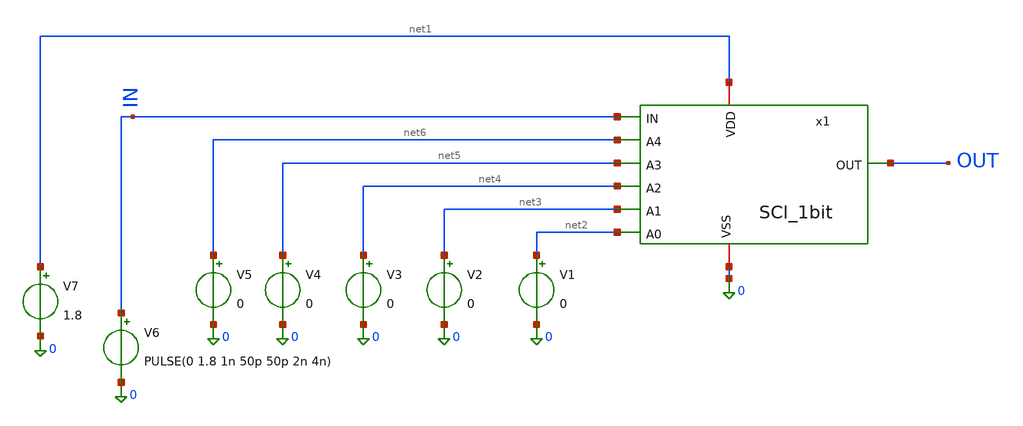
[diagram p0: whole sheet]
** sch_path: xschem/schematic/SCI_DCDL/TG_SCI/TB_SCI_MOS.sch
**.subckt TB_SCI_MOS
x1 net1 IN OUT 0 net6 net5 net4 net3 net2 SCI_1bit
V1 net2 0 0
V2 net3 0 0
V3 net4 0 0
V4 net5 0 0
V5 net6 0 0
V6 IN 0 PULSE(0 1.8 1n 50p 50p 2n 4n)
V7 net1 0 1.8
**** begin user architecture code

** opencircuitdesign pdks install
.lib $::SKYWATER_MODELS/sky130.lib.spice tt



.option rshunt=1e12
.tran 2p 25n

.control
save v(IN) v(OUT)

* Output file
echo code t_rise_ps t_fall_ps t_pd_ps > /home/xiaohi/Projects/sky130_dcdl/results/csv/sci5_delay.dat

* Sweep 5-bit: 00000 -> 11111
foreach b4 0 1
 foreach b3 0 1
  foreach b2 0 1
   foreach b1 0 1
    foreach b0 0 1

     * Convert bits to voltage
     let v0 = 1.8 * $b0
     let v1 = 1.8 * $b1
     let v2 = 1.8 * $b2
     let v3 = 1.8 * $b3
     let v4 = 1.8 * $b4

     * Set control voltage
     alter V1 $&v0
     alter V2 $&v1
     alter V3 $&v2
     alter V4 $&v3
     alter V5 $&v4

     * Run transient simulation
     run

     * Measure propagation delay
     meas tran t_rise TRIG v(IN) VAL=0.9 RISE=2 TARG v(OUT) VAL=0.9 RISE=2
     meas tran t_fall TRIG v(IN) VAL=0.9 FALL=2 TARG v(OUT) VAL=0.9 FALL=2

     * Calculate code and delay in ps
     let code = 16 * $b4 + 8 * $b3 + 4 * $b2 + 2 * $b1 + $b0
     let rise_ps = t_rise * 1e12
     let fall_ps = t_fall * 1e12
     let pd_ps = (rise_ps + fall_ps)/2

     * Append result to file
     echo $&code $&rise_ps $&fall_ps $&pd_ps >>
+ /home/xiaohi/Projects/sky130_dcdl/results/csv/sci5_delay.dat

    end
   end
  end
 end
end

echo Sweep completed: 32 codes
.endc


**** end user architecture code
**.ends

* expanding   symbol:  /home/xiaohi/Projects/sky130_dcdl/xschem/schematic/SCI_DCDL/SCI_1bit.sym # of
*+ pins=9
** sym_path: xschem/schematic/SCI_DCDL/mos_capacitive_baseline/SCI_1bit.sym
** sch_path: xschem/schematic/SCI_DCDL/mos_capacitive_baseline/SCI_1bit.sch
.subckt SCI_1bit VDD IN OUT VSS A4 A3 A2 A1 A0
*.ipin IN
*.opin OUT
*.iopin VDD
*.iopin VSS
*.ipin A4
*.ipin A3
*.ipin A2
*.ipin A1
*.ipin A0
XM1 net1 IN VSS VSS sky130_fd_pr__nfet_01v8 L=0.15 W=2 nf=1 ad='int((1 + 1)/2) * 2 / 1 * 0.29' as='int((1 + 2)/2) * 2 / 1 * 0.29'
+ pd='2*int((1 + 1)/2) * (2 / 1 + 0.29)' ps='2*int((1 + 2)/2) * (2 / 1 + 0.29)' nrd='0.29 / 2 ' nrs='0.29 / 2 '
+ sa=0 sb=0 sd=0 mult=1 m=1
XM3 OUT net1 VSS VSS sky130_fd_pr__nfet_01v8 L=0.15 W=1 nf=1 ad='int((1 + 1)/2) * 1 / 1 * 0.29' as='int((1 + 2)/2) * 1 / 1 * 0.29'
+ pd='2*int((1 + 1)/2) * (1 / 1 + 0.29)' ps='2*int((1 + 2)/2) * (1 / 1 + 0.29)' nrd='0.29 / 1 ' nrs='0.29 / 1 '
+ sa=0 sb=0 sd=0 mult=1 m=1
XM5 net1 IN VDD VDD sky130_fd_pr__pfet_01v8 L=0.15 W=5 nf=1 ad='int((1 + 1)/2) * 5 / 1 * 0.29' as='int((1 + 2)/2) * 5 / 1 * 0.29'
+ pd='2*int((1 + 1)/2) * (5 / 1 + 0.29)' ps='2*int((1 + 2)/2) * (5 / 1 + 0.29)' nrd='0.29 / 5 ' nrs='0.29 / 5 '
+ sa=0 sb=0 sd=0 mult=1 m=1
XM2 OUT net1 VDD VDD sky130_fd_pr__pfet_01v8 L=0.15 W=2.5 nf=1 ad='int((1 + 1)/2) * 2.5 / 1 * 0.29' as='int((1 + 2)/2) * 2.5 / 1 * 0.29'
+ pd='2*int((1 + 1)/2) * (2.5 / 1 + 0.29)' ps='2*int((1 + 2)/2) * (2.5 / 1 + 0.29)' nrd='0.29 / 2.5 ' nrs='0.29 / 2.5 '
+ sa=0 sb=0 sd=0 mult=1 m=1
XM4 net1 A4 net2 VSS sky130_fd_pr__nfet_01v8 L=0.15 W=0.42 nf=1 ad='int((1 + 1)/2) * 0.42 / 1 * 0.29'
+ as='int((1 + 2)/2) * 0.42 / 1 * 0.29' pd='2*int((1 + 1)/2) * (0.42 / 1 + 0.29)' ps='2*int((1 + 2)/2) * (0.42 / 1 + 0.29)'
+ nrd='0.29 / 0.42 ' nrs='0.29 / 0.42 ' sa=0 sb=0 sd=0 mult=1 m=1
XM6 net1 A3 net3 VSS sky130_fd_pr__nfet_01v8 L=0.15 W=0.42 nf=1 ad='int((1 + 1)/2) * 0.42 / 1 * 0.29'
+ as='int((1 + 2)/2) * 0.42 / 1 * 0.29' pd='2*int((1 + 1)/2) * (0.42 / 1 + 0.29)' ps='2*int((1 + 2)/2) * (0.42 / 1 + 0.29)'
+ nrd='0.29 / 0.42 ' nrs='0.29 / 0.42 ' sa=0 sb=0 sd=0 mult=1 m=1
XM7 net1 A2 net4 VSS sky130_fd_pr__nfet_01v8 L=0.15 W=0.42 nf=1 ad='int((1 + 1)/2) * 0.42 / 1 * 0.29'
+ as='int((1 + 2)/2) * 0.42 / 1 * 0.29' pd='2*int((1 + 1)/2) * (0.42 / 1 + 0.29)' ps='2*int((1 + 2)/2) * (0.42 / 1 + 0.29)'
+ nrd='0.29 / 0.42 ' nrs='0.29 / 0.42 ' sa=0 sb=0 sd=0 mult=1 m=1
XM8 net1 A1 net5 VSS sky130_fd_pr__nfet_01v8 L=0.15 W=0.42 nf=1 ad='int((1 + 1)/2) * 0.42 / 1 * 0.29'
+ as='int((1 + 2)/2) * 0.42 / 1 * 0.29' pd='2*int((1 + 1)/2) * (0.42 / 1 + 0.29)' ps='2*int((1 + 2)/2) * (0.42 / 1 + 0.29)'
+ nrd='0.29 / 0.42 ' nrs='0.29 / 0.42 ' sa=0 sb=0 sd=0 mult=1 m=1
XM9 net1 A0 net6 VSS sky130_fd_pr__nfet_01v8 L=0.15 W=0.42 nf=1 ad='int((1 + 1)/2) * 0.42 / 1 * 0.29'
+ as='int((1 + 2)/2) * 0.42 / 1 * 0.29' pd='2*int((1 + 1)/2) * (0.42 / 1 + 0.29)' ps='2*int((1 + 2)/2) * (0.42 / 1 + 0.29)'
+ nrd='0.29 / 0.42 ' nrs='0.29 / 0.42 ' sa=0 sb=0 sd=0 mult=1 m=1
XM10 VSS net2 VSS VSS sky130_fd_pr__nfet_01v8 L=0.15 W=8 nf=1 ad='int((1 + 1)/2) * 8 / 1 * 0.29' as='int((1 + 2)/2) * 8 / 1 * 0.29'
+ pd='2*int((1 + 1)/2) * (8 / 1 + 0.29)' ps='2*int((1 + 2)/2) * (8 / 1 + 0.29)' nrd='0.29 / 8 ' nrs='0.29 / 8 '
+ sa=0 sb=0 sd=0 mult=1 m=1
XM11 net7 net3 net7 net7 sky130_fd_pr__nfet_01v8 L=0.15 W=4 nf=1 ad='int((1 + 1)/2) * 4 / 1 * 0.29' as='int((1 + 2)/2) * 4 / 1 * 0.29'
+ pd='2*int((1 + 1)/2) * (4 / 1 + 0.29)' ps='2*int((1 + 2)/2) * (4 / 1 + 0.29)' nrd='0.29 / 4 ' nrs='0.29 / 4 '
+ sa=0 sb=0 sd=0 mult=1 m=1
XM12 VSS net4 VSS VSS sky130_fd_pr__nfet_01v8 L=0.15 W=2 nf=1 ad='int((1 + 1)/2) * 2 / 1 * 0.29' as='int((1 + 2)/2) * 2 / 1 * 0.29'
+ pd='2*int((1 + 1)/2) * (2 / 1 + 0.29)' ps='2*int((1 + 2)/2) * (2 / 1 + 0.29)' nrd='0.29 / 2 ' nrs='0.29 / 2 '
+ sa=0 sb=0 sd=0 mult=1 m=1
XM13 VSS net5 VSS VSS sky130_fd_pr__nfet_01v8 L=0.15 W=1 nf=1 ad='int((1 + 1)/2) * 1 / 1 * 0.29' as='int((1 + 2)/2) * 1 / 1 * 0.29'
+ pd='2*int((1 + 1)/2) * (1 / 1 + 0.29)' ps='2*int((1 + 2)/2) * (1 / 1 + 0.29)' nrd='0.29 / 1 ' nrs='0.29 / 1 '
+ sa=0 sb=0 sd=0 mult=1 m=1
XM14 VSS net6 VSS VSS sky130_fd_pr__nfet_01v8 L=0.15 W=0.5 nf=1 ad='int((1 + 1)/2) * 0.5 / 1 * 0.29'
+ as='int((1 + 2)/2) * 0.5 / 1 * 0.29' pd='2*int((1 + 1)/2) * (0.5 / 1 + 0.29)' ps='2*int((1 + 2)/2) * (0.5 / 1 + 0.29)'
+ nrd='0.29 / 0.5 ' nrs='0.29 / 0.5 ' sa=0 sb=0 sd=0 mult=1 m=1
.ends

.end
